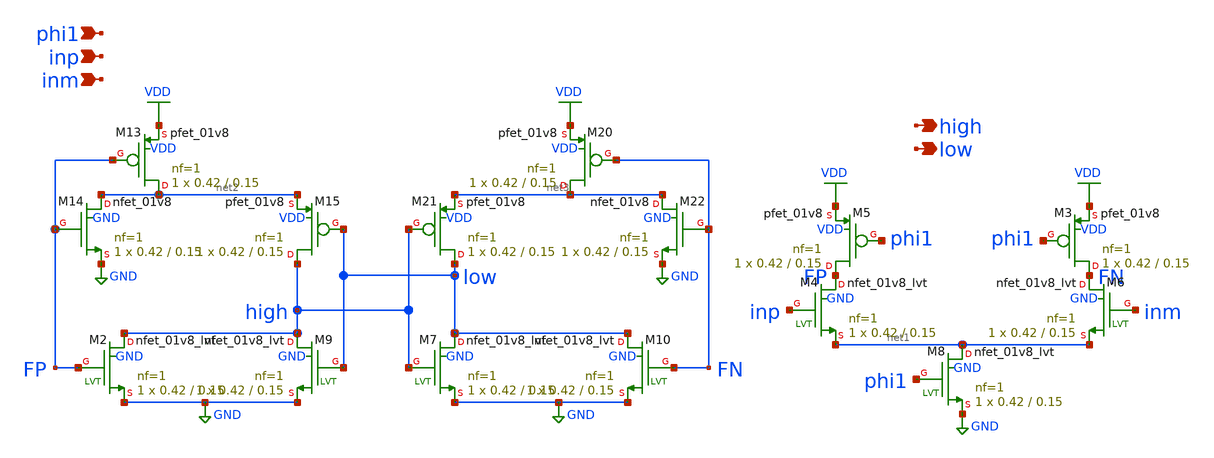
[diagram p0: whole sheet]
** sch_path: xschem/tryandtest/archive/comparator_type_2.sch
**.subckt comparator_type_2 phi1 high inp inm low
*.ipin phi1
*.opin high
*.ipin inp
*.ipin inm
*.opin low
XM3 FN phi1 VDD VDD sky130_fd_pr__pfet_01v8 L=0.15 W=0.42 nf=1 ad='int((nf+1)/2) * W/nf * 0.29' as='int((nf+2)/2) * W/nf * 0.29'
+ pd='2*int((nf+1)/2) * (W/nf + 0.29)' ps='2*int((nf+2)/2) * (W/nf + 0.29)' nrd='0.29 / W' nrs='0.29 / W'
+ sa=0 sb=0 sd=0 mult=1 m=1
XM5 FP phi1 VDD VDD sky130_fd_pr__pfet_01v8 L=0.15 W=0.42 nf=1 ad='int((nf+1)/2) * W/nf * 0.29' as='int((nf+2)/2) * W/nf * 0.29'
+ pd='2*int((nf+1)/2) * (W/nf + 0.29)' ps='2*int((nf+2)/2) * (W/nf + 0.29)' nrd='0.29 / W' nrs='0.29 / W'
+ sa=0 sb=0 sd=0 mult=1 m=1
XM13 net2 FP VDD VDD sky130_fd_pr__pfet_01v8 L=0.15 W=0.42 nf=1 ad='int((nf+1)/2) * W/nf * 0.29' as='int((nf+2)/2) * W/nf * 0.29'
+ pd='2*int((nf+1)/2) * (W/nf + 0.29)' ps='2*int((nf+2)/2) * (W/nf + 0.29)' nrd='0.29 / W' nrs='0.29 / W'
+ sa=0 sb=0 sd=0 mult=1 m=1
XM14 net2 FP GND GND sky130_fd_pr__nfet_01v8 L=0.15 W=0.42 nf=1 ad='int((nf+1)/2) * W/nf * 0.29' as='int((nf+2)/2) * W/nf * 0.29'
+ pd='2*int((nf+1)/2) * (W/nf + 0.29)' ps='2*int((nf+2)/2) * (W/nf + 0.29)' nrd='0.29 / W' nrs='0.29 / W'
+ sa=0 sb=0 sd=0 mult=1 m=1
XM15 high low net2 VDD sky130_fd_pr__pfet_01v8 L=0.15 W=0.42 nf=1 ad='int((nf+1)/2) * W/nf * 0.29' as='int((nf+2)/2) * W/nf * 0.29'
+ pd='2*int((nf+1)/2) * (W/nf + 0.29)' ps='2*int((nf+2)/2) * (W/nf + 0.29)' nrd='0.29 / W' nrs='0.29 / W'
+ sa=0 sb=0 sd=0 mult=1 m=1
XM20 net3 FN VDD VDD sky130_fd_pr__pfet_01v8 L=0.15 W=0.42 nf=1 ad='int((nf+1)/2) * W/nf * 0.29' as='int((nf+2)/2) * W/nf * 0.29'
+ pd='2*int((nf+1)/2) * (W/nf + 0.29)' ps='2*int((nf+2)/2) * (W/nf + 0.29)' nrd='0.29 / W' nrs='0.29 / W'
+ sa=0 sb=0 sd=0 mult=1 m=1
XM21 low high net3 VDD sky130_fd_pr__pfet_01v8 L=0.15 W=0.42 nf=1 ad='int((nf+1)/2) * W/nf * 0.29' as='int((nf+2)/2) * W/nf * 0.29'
+ pd='2*int((nf+1)/2) * (W/nf + 0.29)' ps='2*int((nf+2)/2) * (W/nf + 0.29)' nrd='0.29 / W' nrs='0.29 / W'
+ sa=0 sb=0 sd=0 mult=1 m=1
XM22 net3 FN GND GND sky130_fd_pr__nfet_01v8 L=0.15 W=0.42 nf=1 ad='int((nf+1)/2) * W/nf * 0.29' as='int((nf+2)/2) * W/nf * 0.29'
+ pd='2*int((nf+1)/2) * (W/nf + 0.29)' ps='2*int((nf+2)/2) * (W/nf + 0.29)' nrd='0.29 / W' nrs='0.29 / W'
+ sa=0 sb=0 sd=0 mult=1 m=1
XM2 high FP GND GND sky130_fd_pr__nfet_01v8_lvt L=0.15 W=0.42 nf=1 ad='int((nf+1)/2) * W/nf * 0.29' as='int((nf+2)/2) * W/nf * 0.29'
+ pd='2*int((nf+1)/2) * (W/nf + 0.29)' ps='2*int((nf+2)/2) * (W/nf + 0.29)' nrd='0.29 / W' nrs='0.29 / W'
+ sa=0 sb=0 sd=0 mult=1 m=1
XM7 low high GND GND sky130_fd_pr__nfet_01v8_lvt L=0.15 W=0.42 nf=1 ad='int((nf+1)/2) * W/nf * 0.29'
+ as='int((nf+2)/2) * W/nf * 0.29' pd='2*int((nf+1)/2) * (W/nf + 0.29)' ps='2*int((nf+2)/2) * (W/nf + 0.29)'
+ nrd='0.29 / W' nrs='0.29 / W' sa=0 sb=0 sd=0 mult=1 m=1
XM8 net1 phi1 GND GND sky130_fd_pr__nfet_01v8_lvt L=0.15 W=0.42 nf=1 ad='int((nf+1)/2) * W/nf * 0.29'
+ as='int((nf+2)/2) * W/nf * 0.29' pd='2*int((nf+1)/2) * (W/nf + 0.29)' ps='2*int((nf+2)/2) * (W/nf + 0.29)'
+ nrd='0.29 / W' nrs='0.29 / W' sa=0 sb=0 sd=0 mult=1 m=1
XM9 high low GND GND sky130_fd_pr__nfet_01v8_lvt L=0.15 W=0.42 nf=1 ad='int((nf+1)/2) * W/nf * 0.29'
+ as='int((nf+2)/2) * W/nf * 0.29' pd='2*int((nf+1)/2) * (W/nf + 0.29)' ps='2*int((nf+2)/2) * (W/nf + 0.29)'
+ nrd='0.29 / W' nrs='0.29 / W' sa=0 sb=0 sd=0 mult=1 m=1
XM10 low FN GND GND sky130_fd_pr__nfet_01v8_lvt L=0.15 W=0.42 nf=1 ad='int((nf+1)/2) * W/nf * 0.29' as='int((nf+2)/2) * W/nf * 0.29'
+ pd='2*int((nf+1)/2) * (W/nf + 0.29)' ps='2*int((nf+2)/2) * (W/nf + 0.29)' nrd='0.29 / W' nrs='0.29 / W'
+ sa=0 sb=0 sd=0 mult=1 m=1
XM4 FP inp net1 GND sky130_fd_pr__nfet_01v8_lvt L=0.15 W=0.42 nf=1 ad='int((nf+1)/2) * W/nf * 0.29' as='int((nf+2)/2) * W/nf * 0.29'
+ pd='2*int((nf+1)/2) * (W/nf + 0.29)' ps='2*int((nf+2)/2) * (W/nf + 0.29)' nrd='0.29 / W' nrs='0.29 / W'
+ sa=0 sb=0 sd=0 mult=1 m=1
XM6 FN inm net1 GND sky130_fd_pr__nfet_01v8_lvt L=0.15 W=0.42 nf=1 ad='int((nf+1)/2) * W/nf * 0.29' as='int((nf+2)/2) * W/nf * 0.29'
+ pd='2*int((nf+1)/2) * (W/nf + 0.29)' ps='2*int((nf+2)/2) * (W/nf + 0.29)' nrd='0.29 / W' nrs='0.29 / W'
+ sa=0 sb=0 sd=0 mult=1 m=1
**.ends
.GLOBAL VDD
.GLOBAL GND
.end
